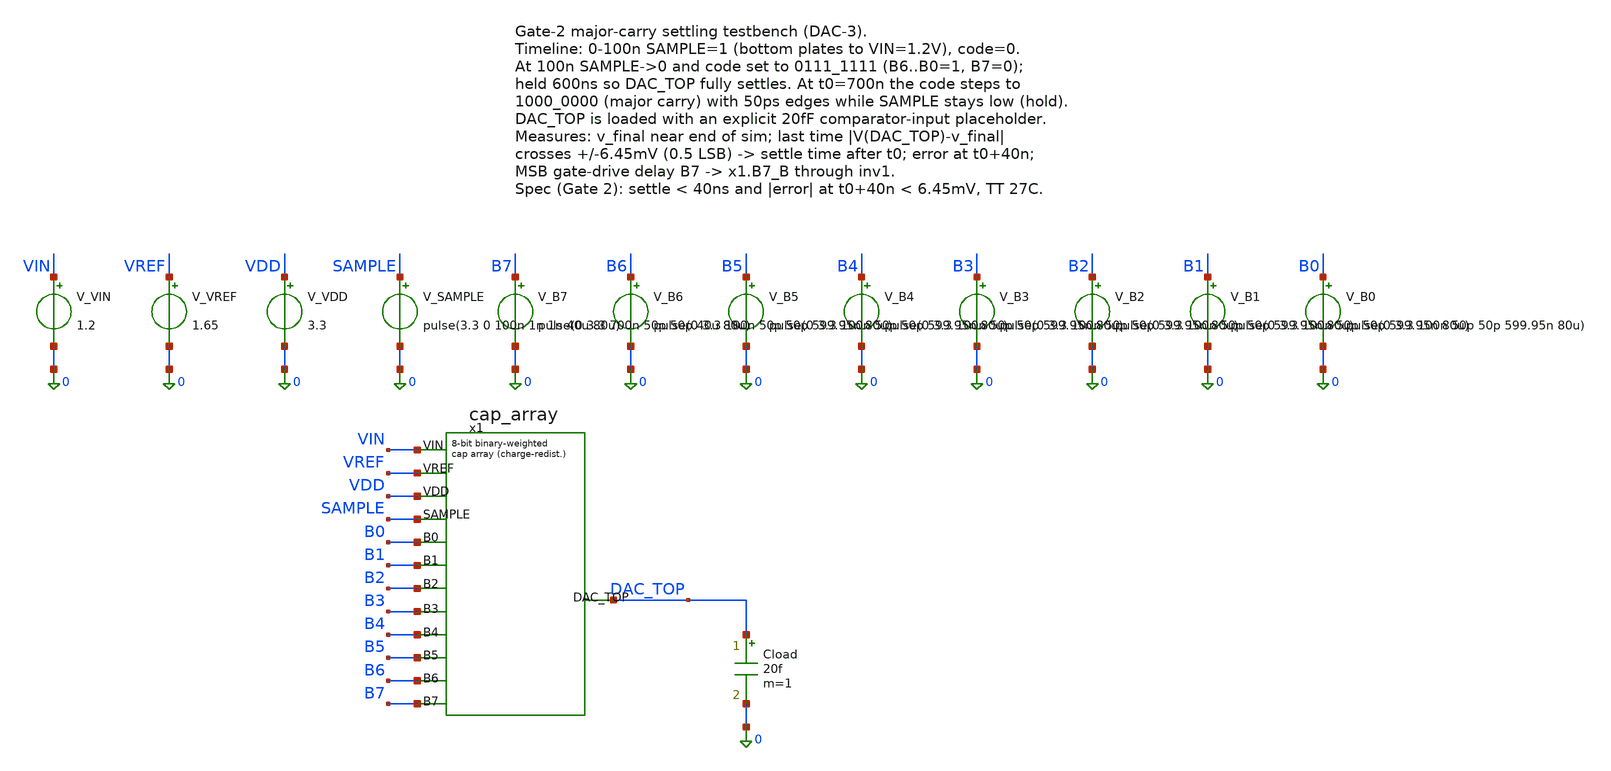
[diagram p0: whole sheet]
** sch_path: dac/sim/tb_major_carry.sch
**.subckt tb_major_carry
V_VIN VIN 0 1.2
V_VREF VREF 0 1.65
V_VDD VDD 0 3.3
V_SAMPLE SAMPLE 0 pulse(3.3 0 100n 1n 1n 40u 80u)
V_B7 B7 0 pulse(0 3.3 700n 50p 50p 40u 80u)
V_B6 B6 0 pulse(0 3.3 100n 50p 50p 599.95n 80u)
V_B5 B5 0 pulse(0 3.3 100n 50p 50p 599.95n 80u)
V_B4 B4 0 pulse(0 3.3 100n 50p 50p 599.95n 80u)
V_B3 B3 0 pulse(0 3.3 100n 50p 50p 599.95n 80u)
V_B2 B2 0 pulse(0 3.3 100n 50p 50p 599.95n 80u)
V_B1 B1 0 pulse(0 3.3 100n 50p 50p 599.95n 80u)
V_B0 B0 0 pulse(0 3.3 100n 50p 50p 599.95n 80u)
Cload DAC_TOP 0 20f m=1
x1 VIN VREF VDD SAMPLE B0 B1 B2 B3 B4 B5 B6 B7 DAC_TOP cap_array
**** begin user architecture code


.param nfet_wid=0.42u nfet_len=0.28u
.param mim_corner_1p0fF=1 mim_corner_1p5fF=1 mim_corner_2p0fF=1
.param mc_c_cox_1p0fF=0 mc_c_cox_1p5fF=0 mc_c_cox_2p0fF=0
.param var_vth=0 var_k=0
.lib /foss/pdks/gf180mcuD/libs.tech/ngspice/sm141064.ngspice typical
.lib /foss/pdks/gf180mcuD/libs.tech/ngspice/sm141064.ngspice cap_mim
.include /foss/pdks/gf180mcuD/libs.tech/ngspice/design.ngspice
.options savecurrents
.control
save all
tran 0.02n 1.05u
* final settled value near end of sim (t0=700n, so this is t0+340n)
meas tran v_final FIND v(DAC_TOP) AT=1.04u
let verr = v(DAC_TOP) - v_final
* settle time: LAST crossing of the +/-0.5LSB (6.45mV) band around v_final
meas tran t_hi_last WHEN verr=6.45m CROSS=LAST
meas tran t_lo_last WHEN verr=-6.45m CROSS=LAST
* value and error exactly at t0+40n
meas tran v_at40 FIND v(DAC_TOP) AT=740n
* MSB gate drive: B7 rises at 700n (50ps edge); B7NAND (bN_bar, direct
* NAND2 output post-TG-integration rework) must fall to turn OFF the MSB
* GND switch. 10%/5% VDD thresholds.
meas tran t_b7b_f90 WHEN v(x1.B7NAND)=0.33 FALL=LAST
meas tran t_b7b_f95 WHEN v(x1.B7NAND)=0.165 FALL=LAST
* bit6 gate drive: B6NAND (bN_bar) must rise to turn ON the 26.88u GND switch
meas tran t_b6b_r90 WHEN v(x1.B6NAND)=2.97 RISE=LAST
echo settle_after_t0_hi_ns:
print (t_hi_last-700e-9)/1e-9
echo settle_after_t0_lo_ns:
print (t_lo_last-700e-9)/1e-9
echo err_at_40n_mV:
print (v_at40-v_final)/1e-3
echo msb_gate_delay_ns_90_95:
print (t_b7b_f90-700e-9)/1e-9 (t_b7b_f95-700e-9)/1e-9
echo b6_gate_delay_ns_90:
print (t_b6b_r90-700e-9)/1e-9
.endc


**** end user architecture code
**.ends
.end
